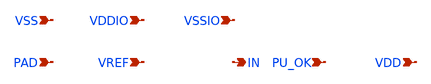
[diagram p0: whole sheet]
** sch_path: sch/pads/gf180mcuD/vref_receiver.sch
**.subckt vref_receiver PAD VREF IN PU_OK VDD VSS VDDIO VSSIO
*.ipin PAD
*.ipin VREF
*.opin IN
*.ipin PU_OK
*.ipin VDD
*.ipin VSS
*.ipin VDDIO
*.ipin VSSIO
**** begin user architecture code


* GENERATED by generator/emit_pads.py -- DO NOT EDIT BY HAND
* backend: gf180mcuD   pdk: gf180mcuD
* topology: specs/pads/topology.yaml v1 (DDR1 VREF receiver, shared across PDKs)
* STATUS: topology_template_only
* SIZE UNITS: topology params are metres; nfet_03v3/pfet_03v3 take w/l in metres
* ESD NOTE: 2-terminal .model diodes; area unit and orientation still need schematic review
* DDR1 decision for this backend: DEFERRED_LONG_TERM
* Long-term plan, not a current deliverable. ARCHITECTURE.md section 1 already says gf180 DDR1 is
*+ not done this period; section 6 now records it as DEFERRED rather than a hard exclusion. Still blocked:
*+ 2.5 V SSTL_2 / VREF IO, no 2.5 V device model, unresolved ck90, and an uncharacterized VREF receiver.
*
* NOT SIMULATABLE. W / I / common-mode / offset / hysteresis are all
* unresolved parameters (required_params.json). ngspice rejects them
* until filled. The ideal tail current source is a placeholder for a
* characterized current mirror, not a designed bias circuit.
*
* Expected includes (NOT bundled): libs.tech/ngspice/sm141064.ngspice ;
*+ libs.tech/ngspice/design.ngspice
*
* Device-instantiation syntax is per backend; the differential-pair
* topology is shared. See specs/pads/devices/<backend>.yaml.
*
* DDR1 read capture topology:
*   PAD and VREF are both VDDIO-domain inputs -> IO devices only.
*   Differential pair + PMOS mirror load -> single-ended -> RX buffer.
*   No DAC, no ADC, no digital output driver on the VREF pad.

* --- differential pair ---
X_VP n_outp PAD n_tail VSSIO nfet_03v3 w=W_VREF_N l=L_PDRV nf=NF_DEVICE m=M_DEVICE
X_VN n_outn VREF n_tail VSSIO nfet_03v3 w=W_VREF_N l=L_PDRV nf=NF_DEVICE m=M_DEVICE
* --- tail current: ideal placeholder ---
I_TAIL n_tail VSSIO DC I_TAIL
* W_TAIL belongs to the real current mirror, TBD.
* --- PMOS current-mirror load ---
X_LP n_outp n_outp VDDIO VDDIO pfet_03v3 w=W_LOAD l=L_PDRV nf=NF_DEVICE m=M_DEVICE
X_LN n_outn n_outp VDDIO VDDIO pfet_03v3 w=W_LOAD l=L_PDRV nf=NF_DEVICE m=M_DEVICE
* --- single-ended output buffer ---
X_RX_N IN n_outn VSSIO VSSIO nfet_03v3 w=W_RX_N l=L_PDRV nf=NF_DEVICE m=M_DEVICE
X_RX_P IN n_outn VDDIO VDDIO pfet_03v3 w=W_RX_P l=L_PDRV nf=NF_DEVICE m=M_DEVICE
* Unresolved: VREF_CM_MIN / VREF_CM_MAX / VREF_OFFSET / VREF_HYST.
* Common-mode range, offset and hysteresis are NOT reported here.

* VREF pad: ESD diodes + metal ONLY. No output driver, no DAC/ADC.
D_VREF_UP VREF VDDIO diode_pd2nw_03v3 area=ESD_AREA_UP
D_VREF_DN VSSIO VREF diode_nd2ps_03v3 area=ESD_AREA_DN


**** end user architecture code
**.ends
.end
